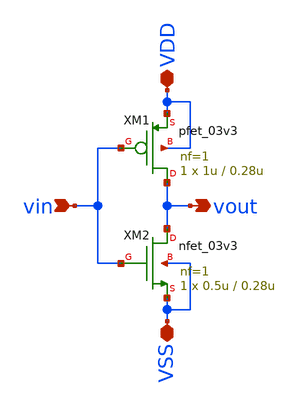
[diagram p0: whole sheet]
** sch_path: sar_logic/sar_designs/inv.sch
**.subckt inv vin vout VDD VSS
*.ipin vin
*.opin vout
*.iopin VDD
*.iopin VSS
XM1 vout vin VDD VDD pfet_03v3 L=0.28u W=1u nf=1 ad='int((nf+1)/2) * W/nf * 0.18u' as='int((nf+2)/2) * W/nf * 0.18u'
+ pd='2*int((nf+1)/2) * (W/nf + 0.18u)' ps='2*int((nf+2)/2) * (W/nf + 0.18u)' nrd='0.18u / W' nrs='0.18u / W'
+ sa=0 sb=0 sd=0 m=1
XM2 vout vin VSS VSS nfet_03v3 L=0.28u W=0.5u nf=1 ad='int((nf+1)/2) * W/nf * 0.18u' as='int((nf+2)/2) * W/nf * 0.18u'
+ pd='2*int((nf+1)/2) * (W/nf + 0.18u)' ps='2*int((nf+2)/2) * (W/nf + 0.18u)' nrd='0.18u / W' nrs='0.18u / W'
+ sa=0 sb=0 sd=0 m=1
**.ends
.end
